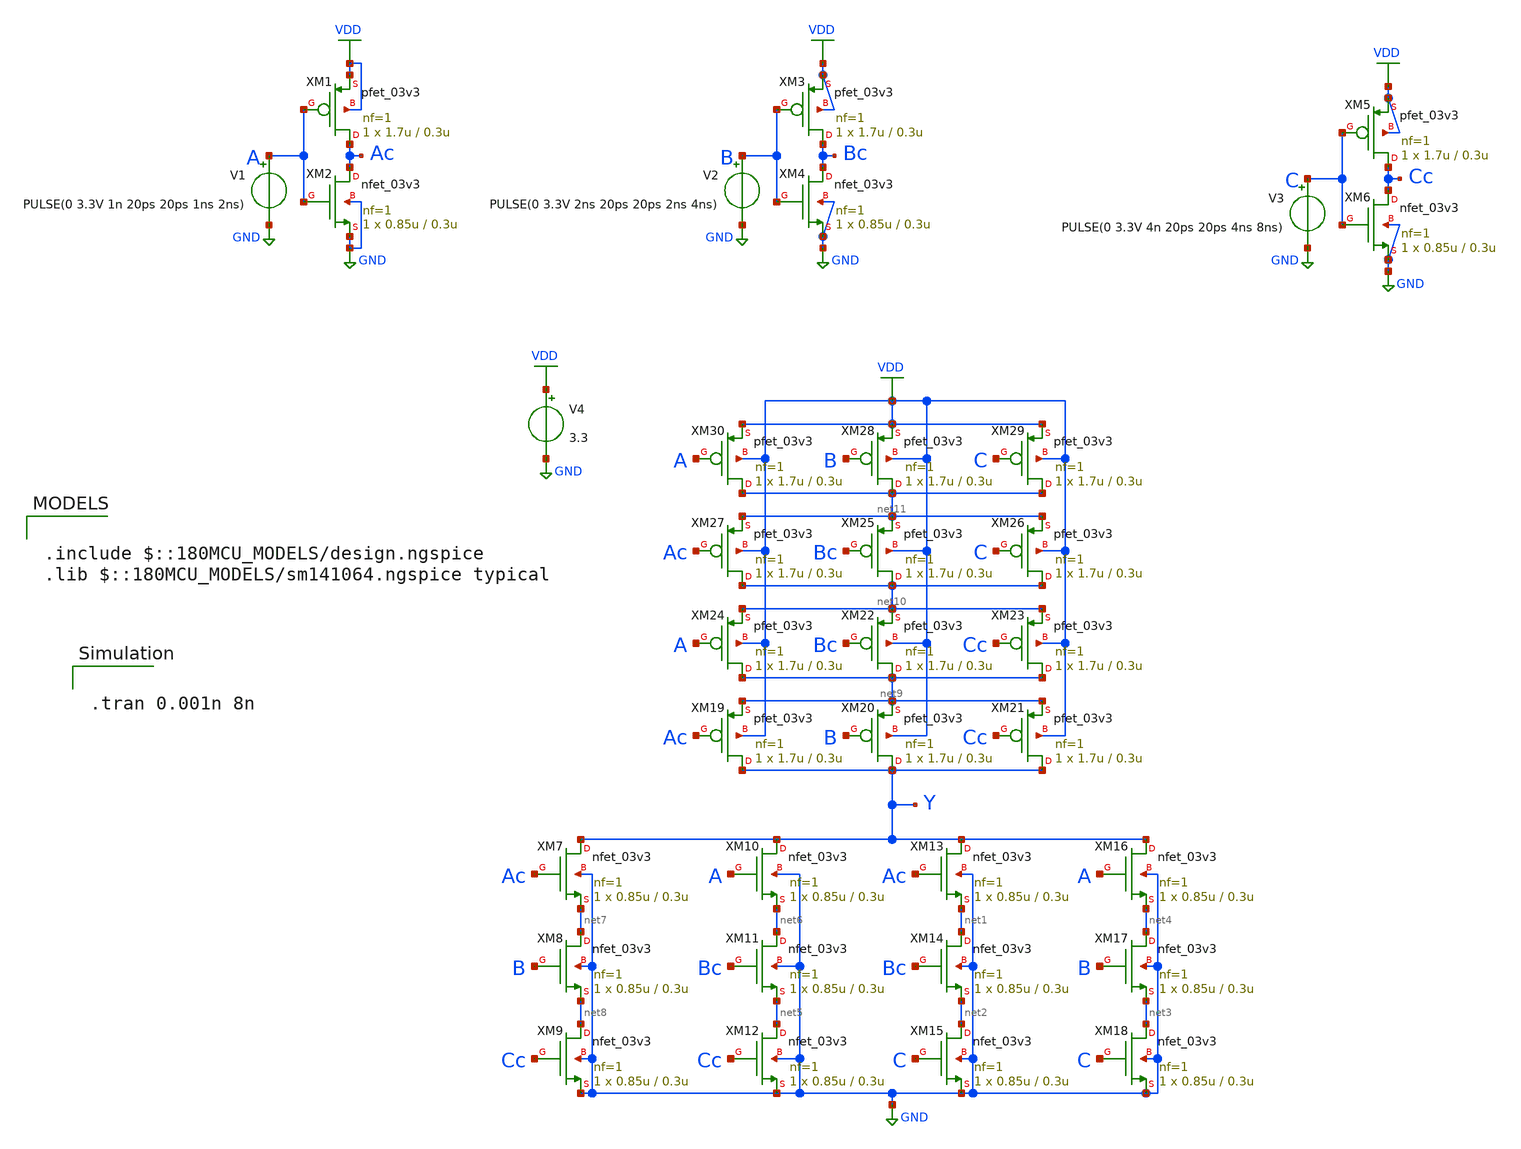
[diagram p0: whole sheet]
** sch_path: xnor3_1.sch
**.subckt xnor3_1
XM1 Ac A VDD VDD pfet_03v3 L=0.3u W=1.7u nf=1 ad='int((nf+1)/2) * W/nf * 0.18u' as='int((nf+2)/2) * W/nf * 0.18u'
+ pd='2*int((nf+1)/2) * (W/nf + 0.18u)' ps='2*int((nf+2)/2) * (W/nf + 0.18u)' nrd='0.18u / W' nrs='0.18u / W'
+ sa=0 sb=0 sd=0 m=1
XM2 Ac A GND GND nfet_03v3 L=0.3u W=0.85u nf=1 ad='int((nf+1)/2) * W/nf * 0.18u' as='int((nf+2)/2) * W/nf * 0.18u'
+ pd='2*int((nf+1)/2) * (W/nf + 0.18u)' ps='2*int((nf+2)/2) * (W/nf + 0.18u)' nrd='0.18u / W' nrs='0.18u / W'
+ sa=0 sb=0 sd=0 m=1
XM3 Bc B VDD VDD pfet_03v3 L=0.3u W=1.7u nf=1 ad='int((nf+1)/2) * W/nf * 0.18u' as='int((nf+2)/2) * W/nf * 0.18u'
+ pd='2*int((nf+1)/2) * (W/nf + 0.18u)' ps='2*int((nf+2)/2) * (W/nf + 0.18u)' nrd='0.18u / W' nrs='0.18u / W'
+ sa=0 sb=0 sd=0 m=1
XM4 Bc B GND GND nfet_03v3 L=0.3u W=0.85u nf=1 ad='int((nf+1)/2) * W/nf * 0.18u' as='int((nf+2)/2) * W/nf * 0.18u'
+ pd='2*int((nf+1)/2) * (W/nf + 0.18u)' ps='2*int((nf+2)/2) * (W/nf + 0.18u)' nrd='0.18u / W' nrs='0.18u / W'
+ sa=0 sb=0 sd=0 m=1
XM5 Cc C VDD VDD pfet_03v3 L=0.3u W=1.7u nf=1 ad='int((nf+1)/2) * W/nf * 0.18u' as='int((nf+2)/2) * W/nf * 0.18u'
+ pd='2*int((nf+1)/2) * (W/nf + 0.18u)' ps='2*int((nf+2)/2) * (W/nf + 0.18u)' nrd='0.18u / W' nrs='0.18u / W'
+ sa=0 sb=0 sd=0 m=1
XM6 Cc C GND GND nfet_03v3 L=0.3u W=0.85u nf=1 ad='int((nf+1)/2) * W/nf * 0.18u' as='int((nf+2)/2) * W/nf * 0.18u'
+ pd='2*int((nf+1)/2) * (W/nf + 0.18u)' ps='2*int((nf+2)/2) * (W/nf + 0.18u)' nrd='0.18u / W' nrs='0.18u / W'
+ sa=0 sb=0 sd=0 m=1
XM7 Y Ac net7 GND nfet_03v3 L=0.3u W=0.85u nf=1 ad='int((nf+1)/2) * W/nf * 0.18u' as='int((nf+2)/2) * W/nf * 0.18u'
+ pd='2*int((nf+1)/2) * (W/nf + 0.18u)' ps='2*int((nf+2)/2) * (W/nf + 0.18u)' nrd='0.18u / W' nrs='0.18u / W'
+ sa=0 sb=0 sd=0 m=1
XM8 net7 B net8 GND nfet_03v3 L=0.3u W=0.85u nf=1 ad='int((nf+1)/2) * W/nf * 0.18u' as='int((nf+2)/2) * W/nf * 0.18u'
+ pd='2*int((nf+1)/2) * (W/nf + 0.18u)' ps='2*int((nf+2)/2) * (W/nf + 0.18u)' nrd='0.18u / W' nrs='0.18u / W'
+ sa=0 sb=0 sd=0 m=1
XM9 net8 Cc GND GND nfet_03v3 L=0.3u W=0.85u nf=1 ad='int((nf+1)/2) * W/nf * 0.18u' as='int((nf+2)/2) * W/nf * 0.18u'
+ pd='2*int((nf+1)/2) * (W/nf + 0.18u)' ps='2*int((nf+2)/2) * (W/nf + 0.18u)' nrd='0.18u / W' nrs='0.18u / W'
+ sa=0 sb=0 sd=0 m=1
XM10 Y A net6 GND nfet_03v3 L=0.3u W=0.85u nf=1 ad='int((nf+1)/2) * W/nf * 0.18u' as='int((nf+2)/2) * W/nf * 0.18u'
+ pd='2*int((nf+1)/2) * (W/nf + 0.18u)' ps='2*int((nf+2)/2) * (W/nf + 0.18u)' nrd='0.18u / W' nrs='0.18u / W'
+ sa=0 sb=0 sd=0 m=1
XM11 net6 Bc net5 GND nfet_03v3 L=0.3u W=0.85u nf=1 ad='int((nf+1)/2) * W/nf * 0.18u' as='int((nf+2)/2) * W/nf * 0.18u'
+ pd='2*int((nf+1)/2) * (W/nf + 0.18u)' ps='2*int((nf+2)/2) * (W/nf + 0.18u)' nrd='0.18u / W' nrs='0.18u / W'
+ sa=0 sb=0 sd=0 m=1
XM12 net5 Cc GND GND nfet_03v3 L=0.3u W=0.85u nf=1 ad='int((nf+1)/2) * W/nf * 0.18u' as='int((nf+2)/2) * W/nf * 0.18u'
+ pd='2*int((nf+1)/2) * (W/nf + 0.18u)' ps='2*int((nf+2)/2) * (W/nf + 0.18u)' nrd='0.18u / W' nrs='0.18u / W'
+ sa=0 sb=0 sd=0 m=1
XM13 Y Ac net1 GND nfet_03v3 L=0.3u W=0.85u nf=1 ad='int((nf+1)/2) * W/nf * 0.18u' as='int((nf+2)/2) * W/nf * 0.18u'
+ pd='2*int((nf+1)/2) * (W/nf + 0.18u)' ps='2*int((nf+2)/2) * (W/nf + 0.18u)' nrd='0.18u / W' nrs='0.18u / W'
+ sa=0 sb=0 sd=0 m=1
XM14 net1 Bc net2 GND nfet_03v3 L=0.3u W=0.85u nf=1 ad='int((nf+1)/2) * W/nf * 0.18u' as='int((nf+2)/2) * W/nf * 0.18u'
+ pd='2*int((nf+1)/2) * (W/nf + 0.18u)' ps='2*int((nf+2)/2) * (W/nf + 0.18u)' nrd='0.18u / W' nrs='0.18u / W'
+ sa=0 sb=0 sd=0 m=1
XM15 net2 C GND GND nfet_03v3 L=0.3u W=0.85u nf=1 ad='int((nf+1)/2) * W/nf * 0.18u' as='int((nf+2)/2) * W/nf * 0.18u'
+ pd='2*int((nf+1)/2) * (W/nf + 0.18u)' ps='2*int((nf+2)/2) * (W/nf + 0.18u)' nrd='0.18u / W' nrs='0.18u / W'
+ sa=0 sb=0 sd=0 m=1
XM16 Y A net4 GND nfet_03v3 L=0.3u W=0.85u nf=1 ad='int((nf+1)/2) * W/nf * 0.18u' as='int((nf+2)/2) * W/nf * 0.18u'
+ pd='2*int((nf+1)/2) * (W/nf + 0.18u)' ps='2*int((nf+2)/2) * (W/nf + 0.18u)' nrd='0.18u / W' nrs='0.18u / W'
+ sa=0 sb=0 sd=0 m=1
XM17 net4 B net3 GND nfet_03v3 L=0.3u W=0.85u nf=1 ad='int((nf+1)/2) * W/nf * 0.18u' as='int((nf+2)/2) * W/nf * 0.18u'
+ pd='2*int((nf+1)/2) * (W/nf + 0.18u)' ps='2*int((nf+2)/2) * (W/nf + 0.18u)' nrd='0.18u / W' nrs='0.18u / W'
+ sa=0 sb=0 sd=0 m=1
XM18 net3 C GND GND nfet_03v3 L=0.3u W=0.85u nf=1 ad='int((nf+1)/2) * W/nf * 0.18u' as='int((nf+2)/2) * W/nf * 0.18u'
+ pd='2*int((nf+1)/2) * (W/nf + 0.18u)' ps='2*int((nf+2)/2) * (W/nf + 0.18u)' nrd='0.18u / W' nrs='0.18u / W'
+ sa=0 sb=0 sd=0 m=1
XM19 Y Ac net9 VDD pfet_03v3 L=0.3u W=1.7u nf=1 ad='int((nf+1)/2) * W/nf * 0.18u' as='int((nf+2)/2) * W/nf * 0.18u'
+ pd='2*int((nf+1)/2) * (W/nf + 0.18u)' ps='2*int((nf+2)/2) * (W/nf + 0.18u)' nrd='0.18u / W' nrs='0.18u / W'
+ sa=0 sb=0 sd=0 m=1
XM20 Y B net9 VDD pfet_03v3 L=0.3u W=1.7u nf=1 ad='int((nf+1)/2) * W/nf * 0.18u' as='int((nf+2)/2) * W/nf * 0.18u'
+ pd='2*int((nf+1)/2) * (W/nf + 0.18u)' ps='2*int((nf+2)/2) * (W/nf + 0.18u)' nrd='0.18u / W' nrs='0.18u / W'
+ sa=0 sb=0 sd=0 m=1
XM21 Y Cc net9 VDD pfet_03v3 L=0.3u W=1.7u nf=1 ad='int((nf+1)/2) * W/nf * 0.18u' as='int((nf+2)/2) * W/nf * 0.18u'
+ pd='2*int((nf+1)/2) * (W/nf + 0.18u)' ps='2*int((nf+2)/2) * (W/nf + 0.18u)' nrd='0.18u / W' nrs='0.18u / W'
+ sa=0 sb=0 sd=0 m=1
XM22 net9 Bc net10 VDD pfet_03v3 L=0.3u W=1.7u nf=1 ad='int((nf+1)/2) * W/nf * 0.18u' as='int((nf+2)/2) * W/nf * 0.18u'
+ pd='2*int((nf+1)/2) * (W/nf + 0.18u)' ps='2*int((nf+2)/2) * (W/nf + 0.18u)' nrd='0.18u / W' nrs='0.18u / W'
+ sa=0 sb=0 sd=0 m=1
XM23 net9 Cc net10 VDD pfet_03v3 L=0.3u W=1.7u nf=1 ad='int((nf+1)/2) * W/nf * 0.18u' as='int((nf+2)/2) * W/nf * 0.18u'
+ pd='2*int((nf+1)/2) * (W/nf + 0.18u)' ps='2*int((nf+2)/2) * (W/nf + 0.18u)' nrd='0.18u / W' nrs='0.18u / W'
+ sa=0 sb=0 sd=0 m=1
XM24 net9 A net10 VDD pfet_03v3 L=0.3u W=1.7u nf=1 ad='int((nf+1)/2) * W/nf * 0.18u' as='int((nf+2)/2) * W/nf * 0.18u'
+ pd='2*int((nf+1)/2) * (W/nf + 0.18u)' ps='2*int((nf+2)/2) * (W/nf + 0.18u)' nrd='0.18u / W' nrs='0.18u / W'
+ sa=0 sb=0 sd=0 m=1
XM25 net10 Bc net11 VDD pfet_03v3 L=0.3u W=1.7u nf=1 ad='int((nf+1)/2) * W/nf * 0.18u' as='int((nf+2)/2) * W/nf * 0.18u'
+ pd='2*int((nf+1)/2) * (W/nf + 0.18u)' ps='2*int((nf+2)/2) * (W/nf + 0.18u)' nrd='0.18u / W' nrs='0.18u / W'
+ sa=0 sb=0 sd=0 m=1
XM26 net10 C net11 VDD pfet_03v3 L=0.3u W=1.7u nf=1 ad='int((nf+1)/2) * W/nf * 0.18u' as='int((nf+2)/2) * W/nf * 0.18u'
+ pd='2*int((nf+1)/2) * (W/nf + 0.18u)' ps='2*int((nf+2)/2) * (W/nf + 0.18u)' nrd='0.18u / W' nrs='0.18u / W'
+ sa=0 sb=0 sd=0 m=1
XM27 net10 Ac net11 VDD pfet_03v3 L=0.3u W=1.7u nf=1 ad='int((nf+1)/2) * W/nf * 0.18u' as='int((nf+2)/2) * W/nf * 0.18u'
+ pd='2*int((nf+1)/2) * (W/nf + 0.18u)' ps='2*int((nf+2)/2) * (W/nf + 0.18u)' nrd='0.18u / W' nrs='0.18u / W'
+ sa=0 sb=0 sd=0 m=1
XM28 net11 B VDD VDD pfet_03v3 L=0.3u W=1.7u nf=1 ad='int((nf+1)/2) * W/nf * 0.18u' as='int((nf+2)/2) * W/nf * 0.18u'
+ pd='2*int((nf+1)/2) * (W/nf + 0.18u)' ps='2*int((nf+2)/2) * (W/nf + 0.18u)' nrd='0.18u / W' nrs='0.18u / W'
+ sa=0 sb=0 sd=0 m=1
XM29 net11 C VDD VDD pfet_03v3 L=0.3u W=1.7u nf=1 ad='int((nf+1)/2) * W/nf * 0.18u' as='int((nf+2)/2) * W/nf * 0.18u'
+ pd='2*int((nf+1)/2) * (W/nf + 0.18u)' ps='2*int((nf+2)/2) * (W/nf + 0.18u)' nrd='0.18u / W' nrs='0.18u / W'
+ sa=0 sb=0 sd=0 m=1
XM30 net11 A VDD VDD pfet_03v3 L=0.3u W=1.7u nf=1 ad='int((nf+1)/2) * W/nf * 0.18u' as='int((nf+2)/2) * W/nf * 0.18u'
+ pd='2*int((nf+1)/2) * (W/nf + 0.18u)' ps='2*int((nf+2)/2) * (W/nf + 0.18u)' nrd='0.18u / W' nrs='0.18u / W'
+ sa=0 sb=0 sd=0 m=1
V1 A GND PULSE(0 3.3V 1n 20ps 20ps 1ns 2ns)
V2 B GND PULSE(0 3.3V 2ns 20ps 20ps 2ns 4ns)
V3 C GND PULSE(0 3.3V 4n 20ps 20ps 4ns 8ns)
V4 VDD GND 3.3
**** begin user architecture code

.tran 0.001n 8n


.include $::180MCU_MODELS/design.ngspice
.lib $::180MCU_MODELS/sm141064.ngspice typical

**** end user architecture code
**.ends
.GLOBAL GND
.GLOBAL VDD
.end
